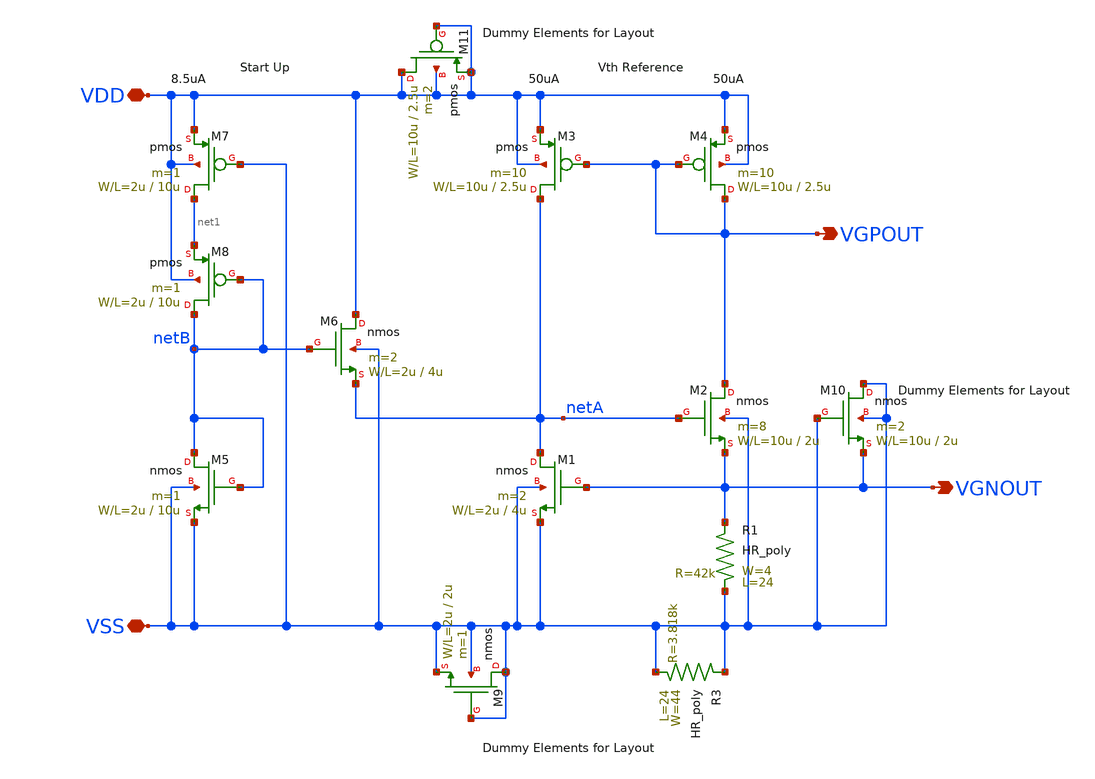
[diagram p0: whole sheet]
** sch_path: member_project/GroupWork/Team_Ando/YuMaehashi/sch/VthRef.sch
**.subckt VthRef VDD VSS VGNOUT VGPOUT
*.iopin VDD
*.iopin VSS
*.opin VGNOUT
*.opin VGPOUT
R1 VSS VGNOUT HR_poly W=4 L=24
M1 netA VGNOUT VSS VSS nmos L=4u W=2u m=2
M2 VGPOUT netA VGNOUT VSS nmos L=2u W=10u m=8
M3 netA VGPOUT VDD VDD pmos L=2.5u W=10u m=10
M4 VGPOUT VGPOUT VDD VDD pmos L=2.5u W=10u m=10
M5 netB netB VSS VSS nmos L=10u W=2u m=1
M6 VDD netB netA VSS nmos L=4u W=2u m=2
M7 net1 VSS VDD VDD pmos L=10u W=2u m=1
M8 netB netB net1 VDD pmos L=10u W=2u m=1
R3 VSS VSS HR_poly W=44 L=24
M9 VSS VSS VSS VSS nmos L=2u W=2u m=1
M10 VSS VSS VGNOUT VSS nmos L=2u W=10u m=2
M11 VDD VDD VDD VDD pmos L=2.5u W=10u m=2
**.ends
.end
